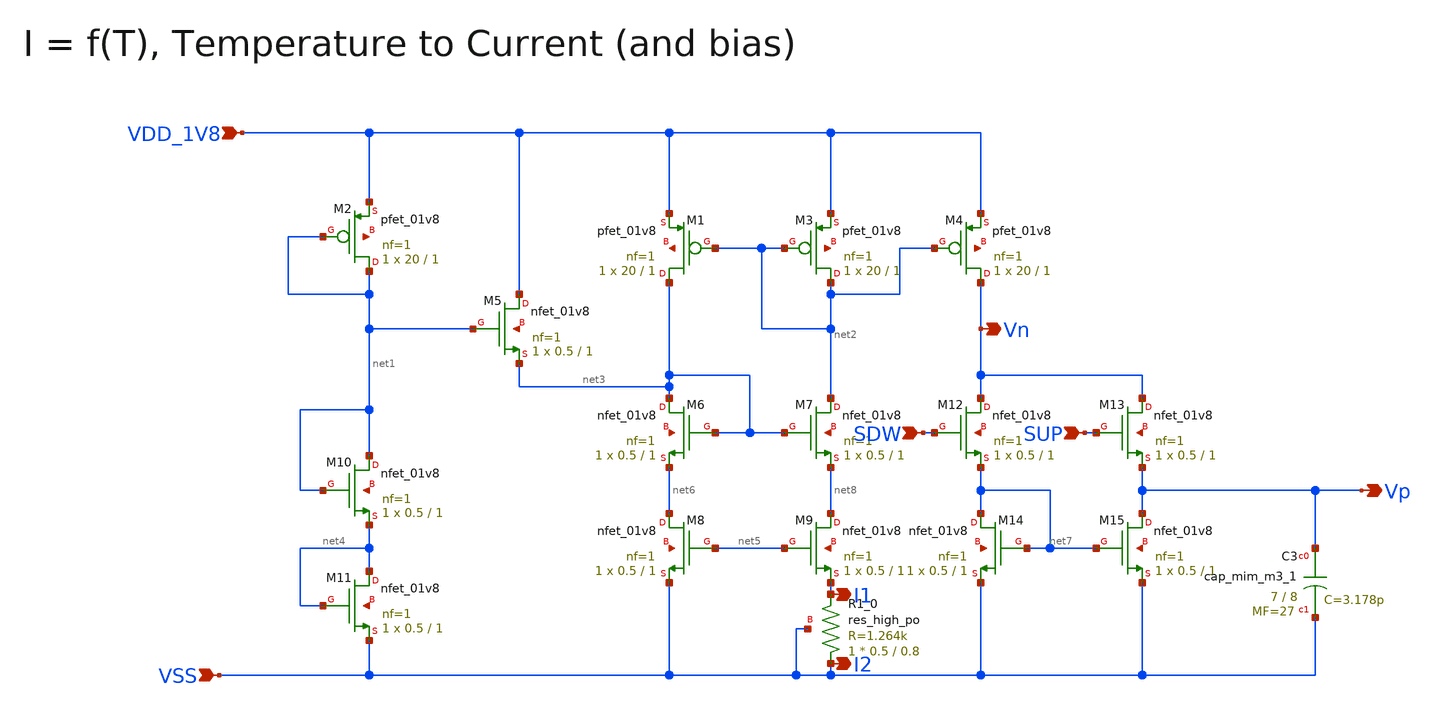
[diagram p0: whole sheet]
** sch_path: design/CNR_GR06_SKY130NM/CNR_GR06.sch
**.subckt CNR_GR06 VDD_1V8 VSS I2 I1 Vn Vp SUP SDW
*.ipin VDD_1V8
*.ipin VSS
*.opin I2
*.opin I1
*.opin Vn
*.opin Vp
*.ipin SUP
*.ipin SDW
XM5 VDD_1V8 net1 net3 net9 sky130_fd_pr__nfet_01v8 L=1 W=0.5 nf=1 ad='int((nf+1)/2) * W/nf * 0.29' as='int((nf+2)/2) * W/nf * 0.29'
+ pd='2*int((nf+1)/2) * (W/nf + 0.29)' ps='2*int((nf+2)/2) * (W/nf + 0.29)' nrd='0.29 / W' nrs='0.29 / W'
+ sa=0 sb=0 sd=0 mult=1 m=1
XM2 net1 net1 VDD_1V8 net10 sky130_fd_pr__pfet_01v8 L=1 W=20 nf=1 ad='int((nf+1)/2) * W/nf * 0.29' as='int((nf+2)/2) * W/nf * 0.29'
+ pd='2*int((nf+1)/2) * (W/nf + 0.29)' ps='2*int((nf+2)/2) * (W/nf + 0.29)' nrd='0.29 / W' nrs='0.29 / W'
+ sa=0 sb=0 sd=0 mult=1 m=1
XM1 net3 net2 VDD_1V8 net11 sky130_fd_pr__pfet_01v8 L=1 W=20 nf=1 ad='int((nf+1)/2) * W/nf * 0.29' as='int((nf+2)/2) * W/nf * 0.29'
+ pd='2*int((nf+1)/2) * (W/nf + 0.29)' ps='2*int((nf+2)/2) * (W/nf + 0.29)' nrd='0.29 / W' nrs='0.29 / W'
+ sa=0 sb=0 sd=0 mult=1 m=1
XM3 net2 net2 VDD_1V8 net12 sky130_fd_pr__pfet_01v8 L=1 W=20 nf=1 ad='int((nf+1)/2) * W/nf * 0.29' as='int((nf+2)/2) * W/nf * 0.29'
+ pd='2*int((nf+1)/2) * (W/nf + 0.29)' ps='2*int((nf+2)/2) * (W/nf + 0.29)' nrd='0.29 / W' nrs='0.29 / W'
+ sa=0 sb=0 sd=0 mult=1 m=1
XM4 Vn net2 VDD_1V8 net13 sky130_fd_pr__pfet_01v8 L=1 W=20 nf=1 ad='int((nf+1)/2) * W/nf * 0.29' as='int((nf+2)/2) * W/nf * 0.29'
+ pd='2*int((nf+1)/2) * (W/nf + 0.29)' ps='2*int((nf+2)/2) * (W/nf + 0.29)' nrd='0.29 / W' nrs='0.29 / W'
+ sa=0 sb=0 sd=0 mult=1 m=1
XM6 net3 net3 net6 net14 sky130_fd_pr__nfet_01v8 L=1 W=0.5 nf=1 ad='int((nf+1)/2) * W/nf * 0.29' as='int((nf+2)/2) * W/nf * 0.29'
+ pd='2*int((nf+1)/2) * (W/nf + 0.29)' ps='2*int((nf+2)/2) * (W/nf + 0.29)' nrd='0.29 / W' nrs='0.29 / W'
+ sa=0 sb=0 sd=0 mult=1 m=1
XM7 net2 net3 net8 net15 sky130_fd_pr__nfet_01v8 L=1 W=0.5 nf=1 ad='int((nf+1)/2) * W/nf * 0.29' as='int((nf+2)/2) * W/nf * 0.29'
+ pd='2*int((nf+1)/2) * (W/nf + 0.29)' ps='2*int((nf+2)/2) * (W/nf + 0.29)' nrd='0.29 / W' nrs='0.29 / W'
+ sa=0 sb=0 sd=0 mult=1 m=1
XM8 net6 net5 VSS net16 sky130_fd_pr__nfet_01v8 L=1 W=0.5 nf=1 ad='int((nf+1)/2) * W/nf * 0.29' as='int((nf+2)/2) * W/nf * 0.29'
+ pd='2*int((nf+1)/2) * (W/nf + 0.29)' ps='2*int((nf+2)/2) * (W/nf + 0.29)' nrd='0.29 / W' nrs='0.29 / W'
+ sa=0 sb=0 sd=0 mult=1 m=1
XM9 net8 net5 I1 net17 sky130_fd_pr__nfet_01v8 L=1 W=0.5 nf=1 ad='int((nf+1)/2) * W/nf * 0.29' as='int((nf+2)/2) * W/nf * 0.29'
+ pd='2*int((nf+1)/2) * (W/nf + 0.29)' ps='2*int((nf+2)/2) * (W/nf + 0.29)' nrd='0.29 / W' nrs='0.29 / W'
+ sa=0 sb=0 sd=0 mult=1 m=1
XM10 net1 net1 net4 net18 sky130_fd_pr__nfet_01v8 L=1 W=0.5 nf=1 ad='int((nf+1)/2) * W/nf * 0.29' as='int((nf+2)/2) * W/nf * 0.29'
+ pd='2*int((nf+1)/2) * (W/nf + 0.29)' ps='2*int((nf+2)/2) * (W/nf + 0.29)' nrd='0.29 / W' nrs='0.29 / W'
+ sa=0 sb=0 sd=0 mult=1 m=1
XM11 net4 net4 VSS net19 sky130_fd_pr__nfet_01v8 L=1 W=0.5 nf=1 ad='int((nf+1)/2) * W/nf * 0.29' as='int((nf+2)/2) * W/nf * 0.29'
+ pd='2*int((nf+1)/2) * (W/nf + 0.29)' ps='2*int((nf+2)/2) * (W/nf + 0.29)' nrd='0.29 / W' nrs='0.29 / W'
+ sa=0 sb=0 sd=0 mult=1 m=1
XM12 Vn SDW net7 net20 sky130_fd_pr__nfet_01v8 L=1 W=0.5 nf=1 ad='int((nf+1)/2) * W/nf * 0.29' as='int((nf+2)/2) * W/nf * 0.29'
+ pd='2*int((nf+1)/2) * (W/nf + 0.29)' ps='2*int((nf+2)/2) * (W/nf + 0.29)' nrd='0.29 / W' nrs='0.29 / W'
+ sa=0 sb=0 sd=0 mult=1 m=1
XM13 Vn SUP Vp net21 sky130_fd_pr__nfet_01v8 L=1 W=0.5 nf=1 ad='int((nf+1)/2) * W/nf * 0.29' as='int((nf+2)/2) * W/nf * 0.29'
+ pd='2*int((nf+1)/2) * (W/nf + 0.29)' ps='2*int((nf+2)/2) * (W/nf + 0.29)' nrd='0.29 / W' nrs='0.29 / W'
+ sa=0 sb=0 sd=0 mult=1 m=1
XM14 net7 net7 VSS net22 sky130_fd_pr__nfet_01v8 L=1 W=0.5 nf=1 ad='int((nf+1)/2) * W/nf * 0.29' as='int((nf+2)/2) * W/nf * 0.29'
+ pd='2*int((nf+1)/2) * (W/nf + 0.29)' ps='2*int((nf+2)/2) * (W/nf + 0.29)' nrd='0.29 / W' nrs='0.29 / W'
+ sa=0 sb=0 sd=0 mult=1 m=1
XM15 Vp net7 VSS net23 sky130_fd_pr__nfet_01v8 L=1 W=0.5 nf=1 ad='int((nf+1)/2) * W/nf * 0.29' as='int((nf+2)/2) * W/nf * 0.29'
+ pd='2*int((nf+1)/2) * (W/nf + 0.29)' ps='2*int((nf+2)/2) * (W/nf + 0.29)' nrd='0.29 / W' nrs='0.29 / W'
+ sa=0 sb=0 sd=0 mult=1 m=1
XC3 Vp VSS sky130_fd_pr__cap_mim_m3_1 W=7 L=8 MF=27 m=27
XR1_0 VSS I1 VSS sky130_fd_pr__res_high_po W=0.5 L=0.8 mult=1 m=1
**.ends
.end
